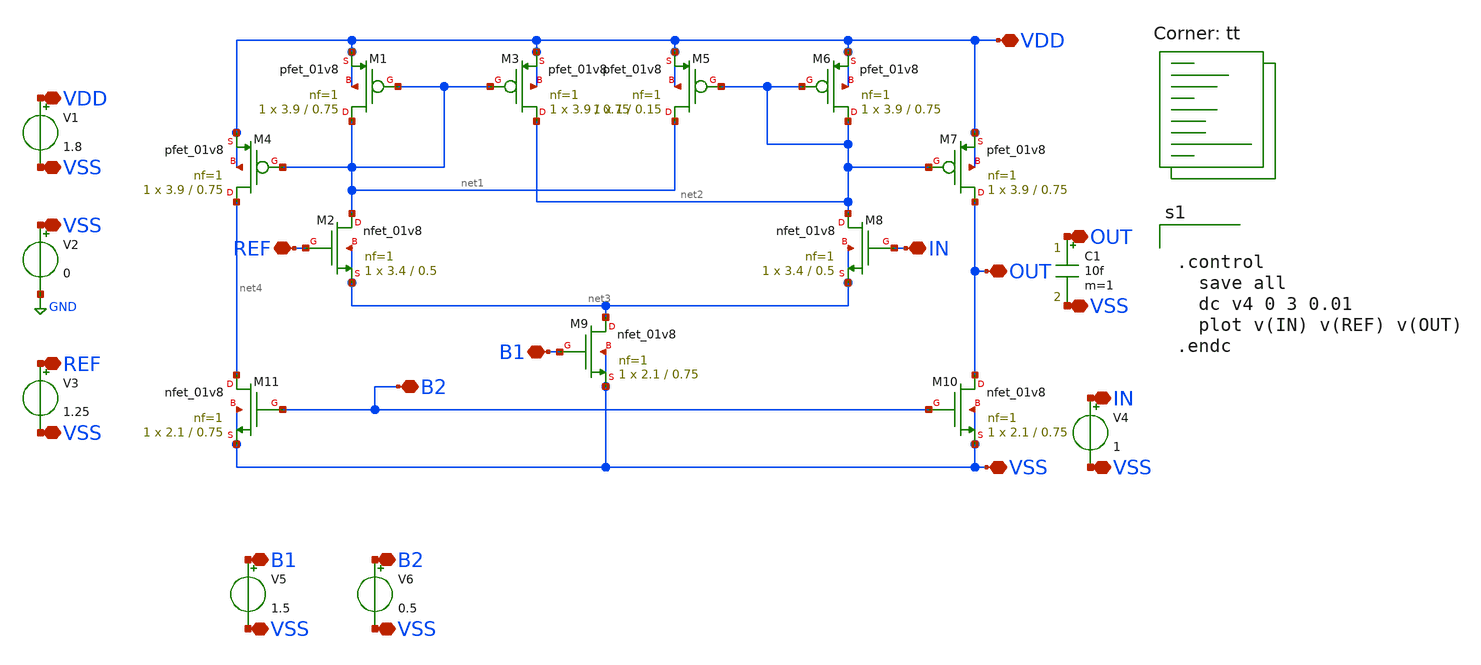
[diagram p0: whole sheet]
** sch_path: cmos_comparator/komparator_histeris_tb.sch
**.subckt komparator_histeris_tb VDD VSS IN REF B2 B1 VDD VSS VSS REF VSS IN VSS OUT OUT VSS B1 VSS
*+ B2 VSS
*.iopin VDD
*.iopin VSS
*.iopin IN
*.iopin REF
*.iopin B2
*.iopin B1
*.iopin VDD
*.iopin VSS
*.iopin VSS
*.iopin REF
*.iopin VSS
*.iopin IN
*.iopin VSS
*.iopin OUT
*.iopin OUT
*.iopin VSS
*.iopin B1
*.iopin VSS
*.iopin B2
*.iopin VSS
XM1 net1 net1 VDD VDD sky130_fd_pr__pfet_01v8 L=0.75 W=3.9 nf=1 ad='int((1 + 1)/2) * 3.9 / 1 * 0.29'
+ as='int((1 + 2)/2) * 3.9 / 1 * 0.29' pd='2*int((1 + 1)/2) * (3.9 / 1 + 0.29)' ps='2*int((1 + 2)/2) * (3.9 / 1 + 0.29)'
+ nrd='0.29 / 3.9 ' nrs='0.29 / 3.9 ' sa=0 sb=0 sd=0 mult=1 m=1
XM2 net1 REF net3 net3 sky130_fd_pr__nfet_01v8 L=0.5 W=3.4 nf=1 ad='int((1 + 1)/2) * 3.4 / 1 * 0.29'
+ as='int((1 + 2)/2) * 3.4 / 1 * 0.29' pd='2*int((1 + 1)/2) * (3.4 / 1 + 0.29)' ps='2*int((1 + 2)/2) * (3.4 / 1 + 0.29)'
+ nrd='0.29 / 3.4 ' nrs='0.29 / 3.4 ' sa=0 sb=0 sd=0 mult=1 m=1
XM3 net2 net1 VDD VDD sky130_fd_pr__pfet_01v8 L=0.75 W=3.9 nf=1 ad='int((1 + 1)/2) * 3.9 / 1 * 0.29'
+ as='int((1 + 2)/2) * 3.9 / 1 * 0.29' pd='2*int((1 + 1)/2) * (3.9 / 1 + 0.29)' ps='2*int((1 + 2)/2) * (3.9 / 1 + 0.29)'
+ nrd='0.29 / 3.9 ' nrs='0.29 / 3.9 ' sa=0 sb=0 sd=0 mult=1 m=1
XM4 net4 net1 VDD VDD sky130_fd_pr__pfet_01v8 L=0.75 W=3.9 nf=1 ad='int((1 + 1)/2) * 3.9 / 1 * 0.29'
+ as='int((1 + 2)/2) * 3.9 / 1 * 0.29' pd='2*int((1 + 1)/2) * (3.9 / 1 + 0.29)' ps='2*int((1 + 2)/2) * (3.9 / 1 + 0.29)'
+ nrd='0.29 / 3.9 ' nrs='0.29 / 3.9 ' sa=0 sb=0 sd=0 mult=1 m=1
XM5 net1 net2 VDD VDD sky130_fd_pr__pfet_01v8 L=0.15 W=1 nf=1 ad='int((1 + 1)/2) * 1 / 1 * 0.29' as='int((1 + 2)/2) * 1 / 1 * 0.29'
+ pd='2*int((1 + 1)/2) * (1 / 1 + 0.29)' ps='2*int((1 + 2)/2) * (1 / 1 + 0.29)' nrd='0.29 / 1 ' nrs='0.29 / 1 '
+ sa=0 sb=0 sd=0 mult=1 m=1
XM6 net2 net2 VDD VDD sky130_fd_pr__pfet_01v8 L=0.75 W=3.9 nf=1 ad='int((1 + 1)/2) * 3.9 / 1 * 0.29'
+ as='int((1 + 2)/2) * 3.9 / 1 * 0.29' pd='2*int((1 + 1)/2) * (3.9 / 1 + 0.29)' ps='2*int((1 + 2)/2) * (3.9 / 1 + 0.29)'
+ nrd='0.29 / 3.9 ' nrs='0.29 / 3.9 ' sa=0 sb=0 sd=0 mult=1 m=1
XM7 OUT net2 VDD VDD sky130_fd_pr__pfet_01v8 L=0.75 W=3.9 nf=1 ad='int((1 + 1)/2) * 3.9 / 1 * 0.29' as='int((1 + 2)/2) * 3.9 / 1 * 0.29'
+ pd='2*int((1 + 1)/2) * (3.9 / 1 + 0.29)' ps='2*int((1 + 2)/2) * (3.9 / 1 + 0.29)' nrd='0.29 / 3.9 ' nrs='0.29 / 3.9 '
+ sa=0 sb=0 sd=0 mult=1 m=1
XM8 net2 IN net3 net3 sky130_fd_pr__nfet_01v8 L=0.5 W=3.4 nf=1 ad='int((1 + 1)/2) * 3.4 / 1 * 0.29' as='int((1 + 2)/2) * 3.4 / 1 * 0.29'
+ pd='2*int((1 + 1)/2) * (3.4 / 1 + 0.29)' ps='2*int((1 + 2)/2) * (3.4 / 1 + 0.29)' nrd='0.29 / 3.4 ' nrs='0.29 / 3.4 '
+ sa=0 sb=0 sd=0 mult=1 m=1
XM9 net3 B1 VSS VSS sky130_fd_pr__nfet_01v8 L=0.75 W=2.1 nf=1 ad='int((1 + 1)/2) * 2.1 / 1 * 0.29' as='int((1 + 2)/2) * 2.1 / 1 * 0.29'
+ pd='2*int((1 + 1)/2) * (2.1 / 1 + 0.29)' ps='2*int((1 + 2)/2) * (2.1 / 1 + 0.29)' nrd='0.29 / 2.1 ' nrs='0.29 / 2.1 '
+ sa=0 sb=0 sd=0 mult=1 m=1
XM10 OUT B2 VSS VSS sky130_fd_pr__nfet_01v8 L=0.75 W=2.1 nf=1 ad='int((1 + 1)/2) * 2.1 / 1 * 0.29' as='int((1 + 2)/2) * 2.1 / 1 * 0.29'
+ pd='2*int((1 + 1)/2) * (2.1 / 1 + 0.29)' ps='2*int((1 + 2)/2) * (2.1 / 1 + 0.29)' nrd='0.29 / 2.1 ' nrs='0.29 / 2.1 '
+ sa=0 sb=0 sd=0 mult=1 m=1
XM11 net4 B2 VSS VSS sky130_fd_pr__nfet_01v8 L=0.75 W=2.1 nf=1 ad='int((1 + 1)/2) * 2.1 / 1 * 0.29' as='int((1 + 2)/2) * 2.1 / 1 * 0.29'
+ pd='2*int((1 + 1)/2) * (2.1 / 1 + 0.29)' ps='2*int((1 + 2)/2) * (2.1 / 1 + 0.29)' nrd='0.29 / 2.1 ' nrs='0.29 / 2.1 '
+ sa=0 sb=0 sd=0 mult=1 m=1
V1 VDD VSS 1.8
V2 VSS GND 0
V3 REF VSS 1.25
V4 IN VSS 1
C1 OUT VSS 10f m=1
V5 B1 VSS 1.5
V6 B2 VSS 0.5
**** begin user architecture code
.lib $::SKYWATER_MODELS/sky130.lib.spice tt


.control
  save all
  dc v4 0 3 0.01
  plot v(IN) v(REF) v(OUT)
.endc


**** end user architecture code
**.ends
.GLOBAL GND
.end
